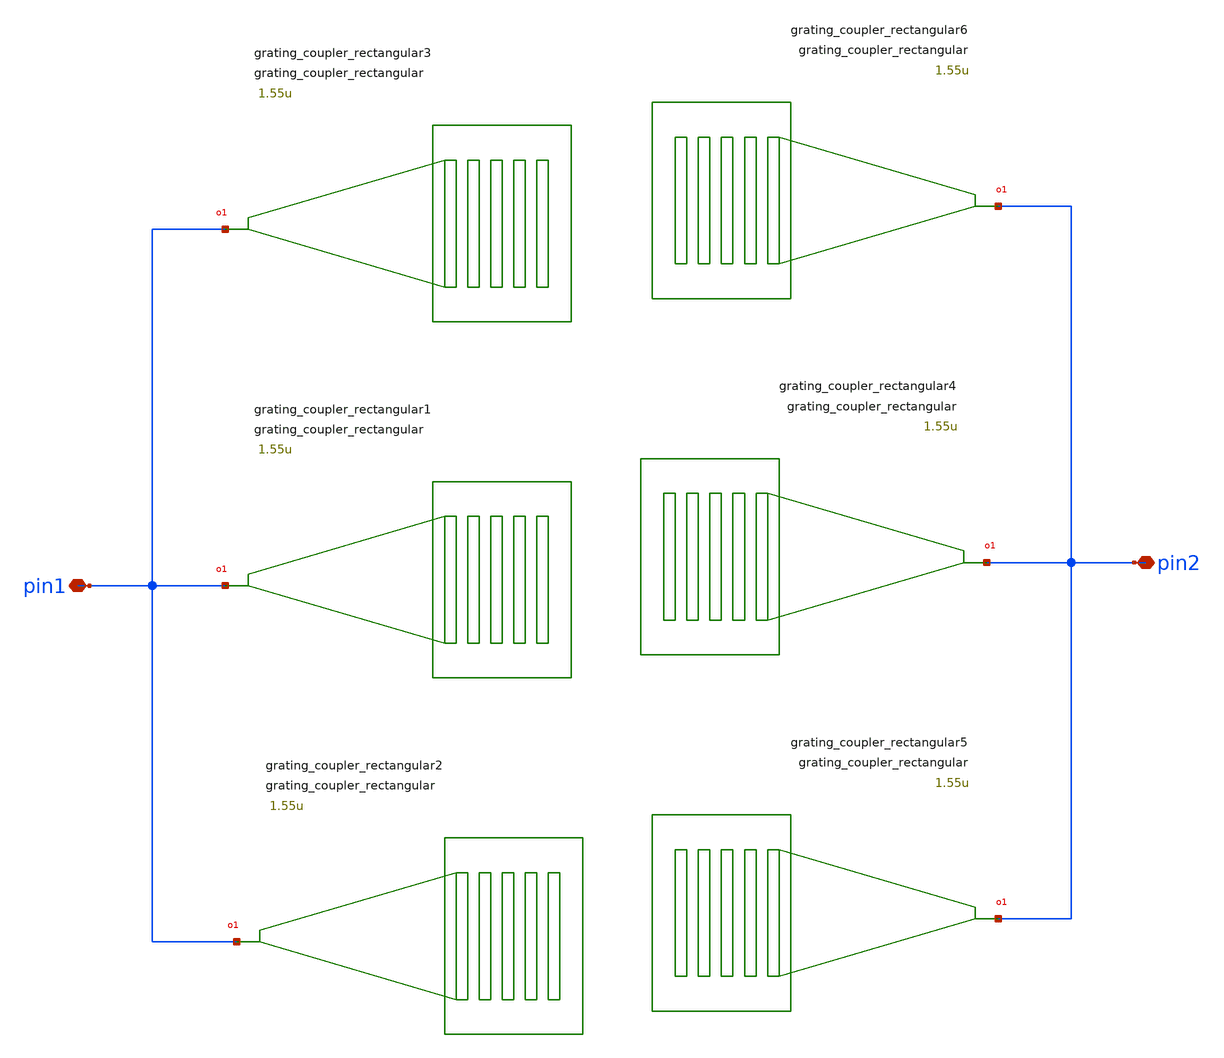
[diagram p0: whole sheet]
** sch_path: xschem/tests/test_sch/test_grating_coupler_rectangular.sch
* Copyright (c) 2024, Mabrains LLC
* Licensed under the GNU Lesser General Public License, Version 3.0 (the "License");
* you may not use this file except in compliance with the License.
* GNU Lesser General Public License
* Version 3, 29 June 2007
* This program is free software: you can redistribute it and/or modify
* it under the terms of the GNU Lesser General Public License as published
* by the Free Software Foundation, either version 3 of the License, or
* (at your option) any later version.
* This program is distributed in the hope that it will be useful,
* but WITHOUT ANY WARRANTY; without even the implied warranty of
* MERCHANTABILITY or FITNESS FOR A PARTICULAR PURPOSE.  See the
* GNU Lesser General Public License for more details.
* You should have received a copy of the GNU Lesser General Public License
* along with this program.  If not, see <https://www.gnu.org/licenses/>.
* SPDX-License-Identifier: LGPL-3.0
**.subckt test_grating_coupler_rectangular pin1 pin2
*.iopin pin1
*.iopin pin2
Pgrating_coupler_rectangular1 pin1 grating_coupler_rectangular n_periods=20 period=0.75
+ fill_factor=0.5 width_grating=11.0u length_taper=150.0u wavelength=1.55u fiber_angle=15 slab_xmin=-1.0u
+ slab_offset=1.0u
Pgrating_coupler_rectangular2 pin1 grating_coupler_rectangular n_periods=20 period=0.75
+ fill_factor=0.5 width_grating=11.0u length_taper=150.0u wavelength=1.55u fiber_angle=15 slab_xmin=-1.0u
+ slab_offset=1.0u
Pgrating_coupler_rectangular3 pin1 grating_coupler_rectangular n_periods=20 period=0.75
+ fill_factor=0.5 width_grating=11.0u length_taper=150.0u wavelength=1.55u fiber_angle=15 slab_xmin=-1.0u
+ slab_offset=1.0u
Pgrating_coupler_rectangular4 pin2 grating_coupler_rectangular n_periods=20 period=0.75
+ fill_factor=0.5 width_grating=11.0u length_taper=150.0u wavelength=1.55u fiber_angle=15 slab_xmin=-1.0u
+ slab_offset=1.0u
Pgrating_coupler_rectangular5 pin2 grating_coupler_rectangular n_periods=20 period=0.75
+ fill_factor=0.5 width_grating=11.0u length_taper=150.0u wavelength=1.55u fiber_angle=15 slab_xmin=-1.0u
+ slab_offset=1.0u
Pgrating_coupler_rectangular6 pin2 grating_coupler_rectangular n_periods=20 period=0.75
+ fill_factor=0.5 width_grating=11.0u length_taper=150.0u wavelength=1.55u fiber_angle=15 slab_xmin=-1.0u
+ slab_offset=1.0u
**.ends
.end
